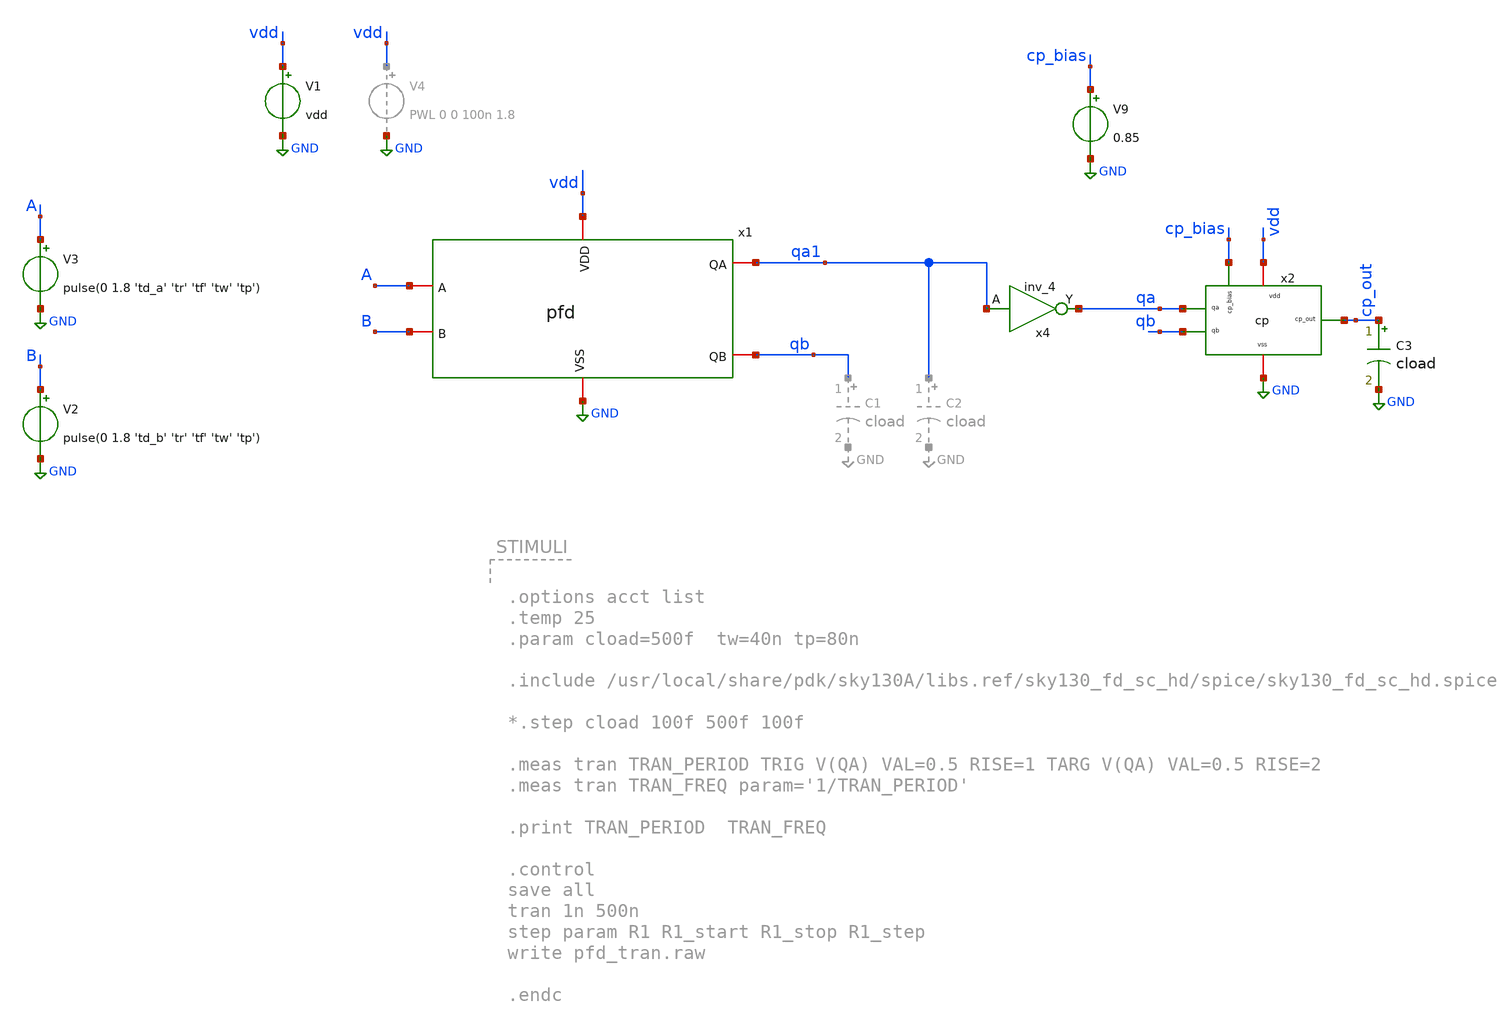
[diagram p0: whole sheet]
** sch_path: xschem/pfd_cp_tran.sch
**.subckt pfd_cp_tran
x1 GND vdd A qa1 qb B pfd
V1 vdd GND vdd
V2 B GND pulse(0 1.8 'td_b' 'tr' 'tf' 'tw' 'tp')
V3 A GND pulse(0 1.8 'td_a' 'tr' 'tf' 'tw' 'tp')
x2 vdd qa cp_out qb GND cp_bias cp
C3 cp_out GND cload m=1
V9 cp_bias GND 0.85
x4 qa1 VSS VSS VDD VDD qa sky130_fd_sc_hd__inv_4
**** begin user architecture code

** opencircuitdesign pdks install
.lib $::SKYWATER_MODELS/sky130.lib.spice tt




.options acct list savecurrents
.temp 25
.param cload=5p vdd=1.8  ibias=10u  low=0  high=1.8  tr=0.1n  tf=0.1n  td_a=200n   td_b=220n  tw=40n
+  tp=80n
******charging
*+ tw_a=50n tp_a=80n
*+ tw_b=0n  tp_b=0n
******discharging
*+ tw_a=0n tp_a=0n
*+ tw_b=50n  tp_b=80n

.include /usr/local/share/pdk/sky130A/libs.ref/sky130_fd_sc_hd/spice/sky130_fd_sc_hd.spice

.ic v(cp_out)=0.9  v(cp_out1)=1.8

*.meas tran TRAN_PERIOD TRIG V(QA) VAL=0.5 RISE=1 TARG V(QA) VAL=0.5 RISE=2
*.meas tran TRAN_FREQ param='1/TRAN_PERIOD'

.print TRAN_PERIOD  TRAN_FREQ
*print @m.x1.xm3.msky130_fd_pr__nfet_01v8[id]  @m.x1.xm4.msky130_fd_pr__pfet_01v8[id]


.control
save all
save @m.x2.xm3.msky130_fd_pr__nfet_01v8[vth]
save @m.x2.xm3.msky130_fd_pr__nfet_01v8[vgs]



op
write pfd_cp_tran.raw
set appendwrite

tran 0.1n 10u
write pfd_cp_tran.raw

print  @m.x1.xm3.msky130_fd_pr__nfet_01v8[vth]
print  @m.x1.xm3.msky130_fd_pr__nfet_01v8[gm]
print  @m.x1.xm3.msky130_fd_pr__nfet_01v8[vgs]

*print x1.bias  x1.n1   x1.cp_out

.endc


**** end user architecture code
**.ends
.GLOBAL GND
.end
